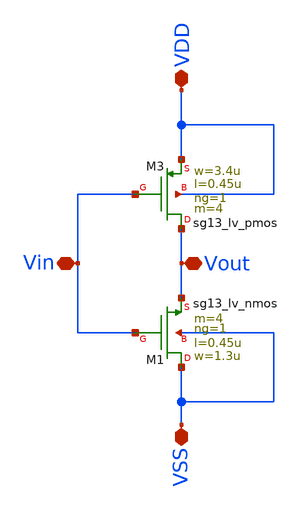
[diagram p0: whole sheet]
** sch_path: unic_cass_wrapper_user_project/ROs_reliability/inverter_RO_rel.sch
**.subckt inverter_RO_rel VDD VSS Vin Vout
*.iopin VDD
*.iopin VSS
*.iopin Vin
*.iopin Vout
XM3 Vout Vin VDD VDD sg13_lv_pmos w=3.4u l=0.45u ng=1 m=4 mm_ok=1
XM1 VSS Vin Vout VSS sg13_lv_nmos w=1.3u l=0.45u ng=1 m=4 mm_ok=1
**.ends
.end
